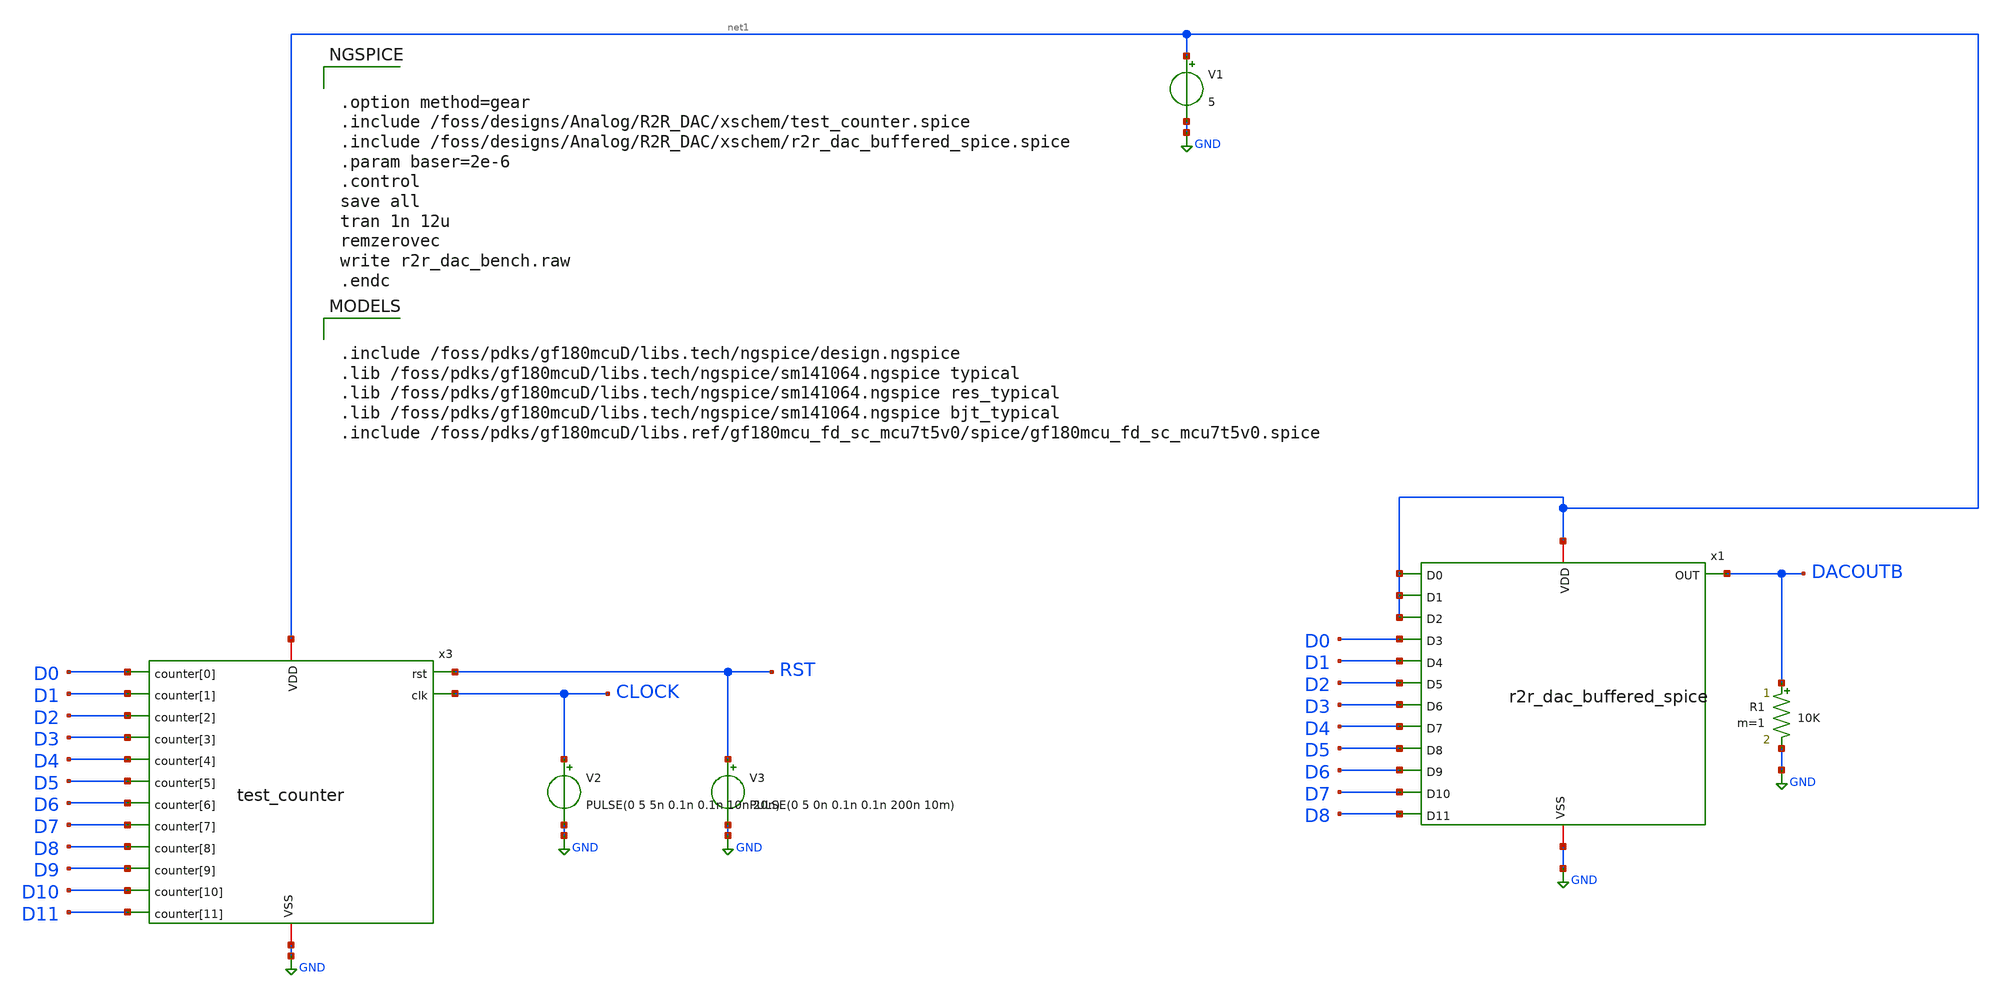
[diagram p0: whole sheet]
** sch_path: macros/Analog/R2R_DAC/xschem/r2r_dac_bench.sch
**.subckt r2r_dac_bench
V1 net1 GND 5
V2 CLOCK GND PULSE(0 5 5n 0.1n 0.1n 10n 20n)
V3 RST GND PULSE(0 5 0n 0.1n 0.1n 200n 10m)
x3 net1 GND CLOCK D0 D10 D11 D1 D2 D3 D4 D5 D6 D7 D8 D9 RST test_counter
R1 DACOUTB GND 10K m=1
x1 DACOUTB net1 net1 net1 D0 D1 D2 D3 D4 D5 D6 D7 D8 net1 GND r2r_dac_buffered_spice
**** begin user architecture code

.include /foss/pdks/gf180mcuD/libs.tech/ngspice/design.ngspice
.lib /foss/pdks/gf180mcuD/libs.tech/ngspice/sm141064.ngspice typical
.lib /foss/pdks/gf180mcuD/libs.tech/ngspice/sm141064.ngspice res_typical
.lib /foss/pdks/gf180mcuD/libs.tech/ngspice/sm141064.ngspice bjt_typical
.include /foss/pdks/gf180mcuD/libs.ref/gf180mcu_fd_sc_mcu7t5v0/spice/gf180mcu_fd_sc_mcu7t5v0.spice



.option method=gear
.include /foss/designs/Analog/R2R_DAC/xschem/test_counter.spice
.include /foss/designs/Analog/R2R_DAC/xschem/r2r_dac_buffered_spice.spice
.param baser=2e-6
.control
save all
tran 1n 12u
remzerovec
write r2r_dac_bench.raw
.endc


**** end user architecture code
**.ends
.GLOBAL GND
.end
